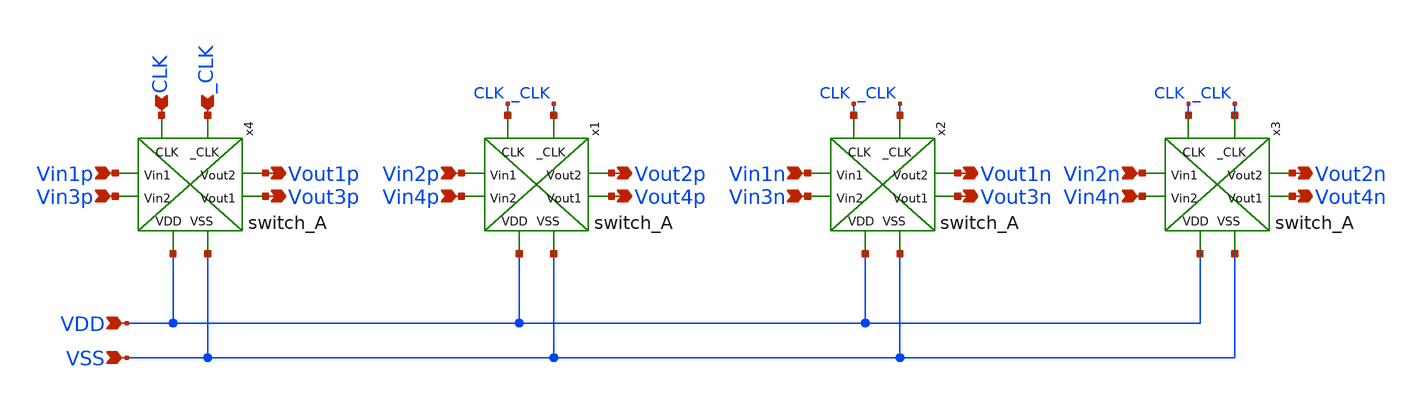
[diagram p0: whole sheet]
** sch_path: ISSCC26/submitted_notebooks/Low Mismatch 4 Channels Instrumentation Amplifier EEG/Chopper Switch/Schmatic and Testbench/switch_C.sch
**.subckt switch_C Vin1p Vin2p Vout1p Vout2p Vin4n Vout4n Vin2n Vout2n Vin3n Vout3n Vin1n Vout1n
*+ Vin4p Vout4p Vin3p Vout3p CLK _CLK VDD VSS
*.ipin Vin1p
*.ipin Vin2p
*.opin Vout1p
*.opin Vout2p
*.ipin Vin4n
*.opin Vout4n
*.ipin Vin2n
*.opin Vout2n
*.ipin Vin3n
*.opin Vout3n
*.ipin Vin1n
*.opin Vout1n
*.ipin Vin4p
*.opin Vout4p
*.ipin Vin3p
*.opin Vout3p
*.ipin CLK
*.ipin _CLK
*.ipin VDD
*.ipin VSS
x1 CLK _CLK Vin2p Vout2p Vout4p Vin4p VDD VSS switch_A
x2 CLK _CLK Vin1n Vout1n Vout3n Vin3n VDD VSS switch_A
x3 CLK _CLK Vin2n Vout2n Vout4n Vin4n VDD VSS switch_A
x4 CLK _CLK Vin1p Vout1p Vout3p Vin3p VDD VSS switch_A
**.ends
.end
